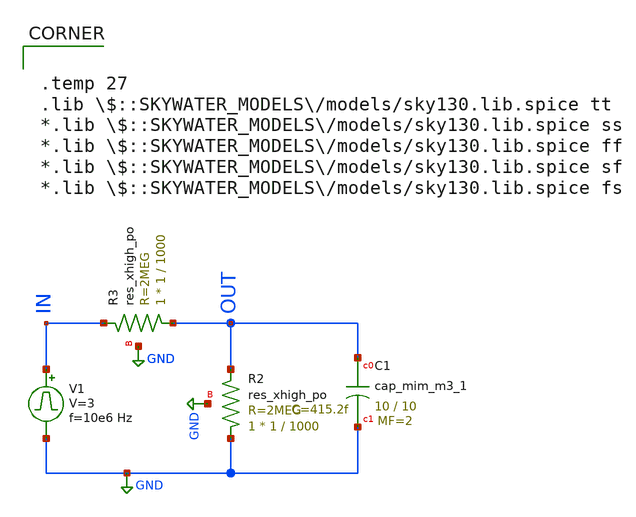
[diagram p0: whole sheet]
** sch_path: test.sch
**.subckt test
XC1 OUT GND sky130_fd_pr__cap_mim_m3_1 W=10 L=10 MF=2 m=2
V1 IN GND pulse 0 3 '0.495/ 10e6 ' '0.01/10e6 ' '0.01/10e6 ' '0.49/10e6 ' '1/10e6 '
XR2 GND OUT GND sky130_fd_pr__res_xhigh_po W=1 L=1000 mult=1 m=1
XR3 OUT IN GND sky130_fd_pr__res_xhigh_po W=1 L=1000 mult=1 m=1
**** begin user architecture code


.save all
.control
tran 1n 1u uic
plot out
.endc



.temp 27
.lib $::SKYWATER_MODELS/models/sky130.lib.spice tt
*.lib $::SKYWATER_MODELS/models/sky130.lib.spice ss
*.lib $::SKYWATER_MODELS/models/sky130.lib.spice ff
*.lib $::SKYWATER_MODELS/models/sky130.lib.spice sf
*.lib $::SKYWATER_MODELS/models/sky130.lib.spice fs

**** end user architecture code
**.ends
.GLOBAL GND
.end
